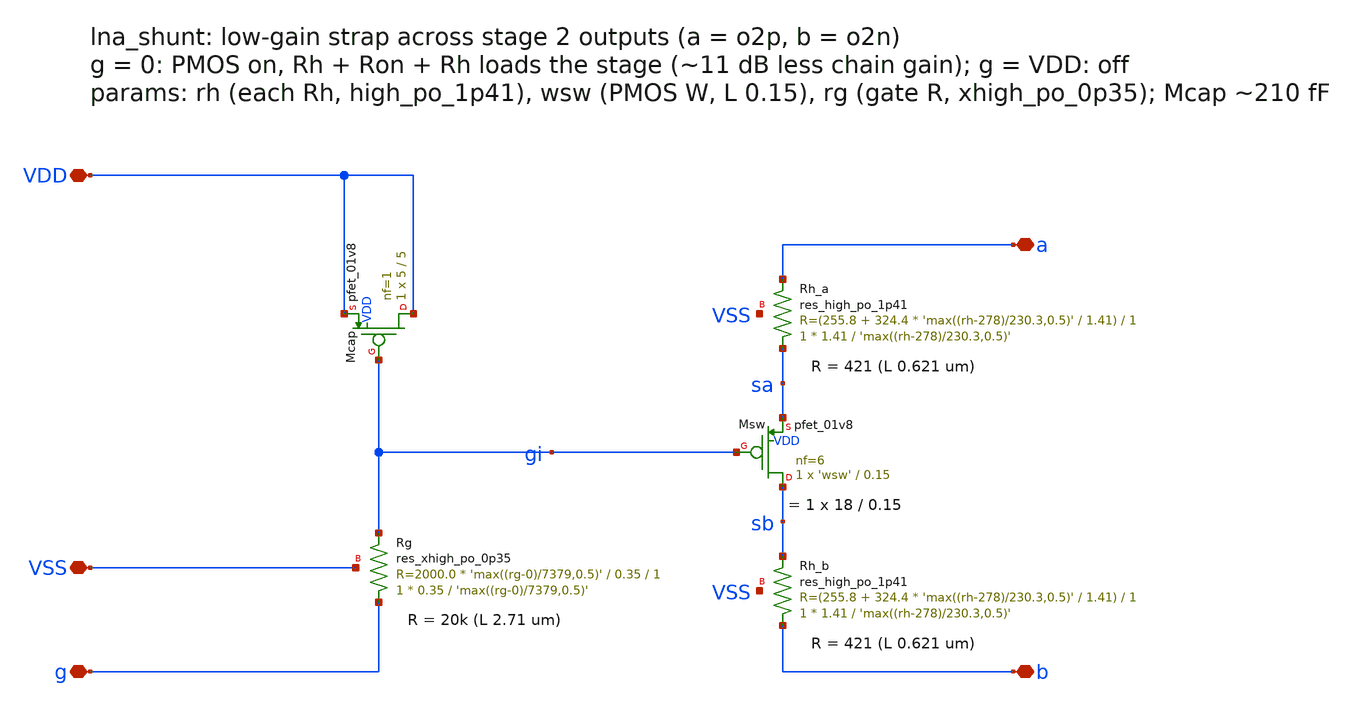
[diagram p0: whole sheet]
** sch_path: xschem/lna_shunt.sch
**.subckt lna_shunt VDD VSS a b g
*.iopin VDD
*.iopin VSS
*.iopin a
*.iopin b
*.iopin g
XRh_a sa a VSS sky130_fd_pr__res_high_po_1p41 L='max((rh-278)/230.3,0.5)' mult=1 m=1
XRh_b b sb VSS sky130_fd_pr__res_high_po_1p41 L='max((rh-278)/230.3,0.5)' mult=1 m=1
XMsw sb gi sa VDD sky130_fd_pr__pfet_01v8 L=0.15 W='wsw' nf=6 ad='int((nf+1)/2) * W/nf * 0.29' as='int((nf+2)/2) * W/nf * 0.29'
+ pd='2*int((nf+1)/2) * (W/nf + 0.29)' ps='2*int((nf+2)/2) * (W/nf + 0.29)' nrd='0.29 / W' nrs='0.29 / W'
+ sa=0 sb=0 sd=0 mult=1 m=1
XRg g gi VSS sky130_fd_pr__res_xhigh_po_0p35 L='max((rg-0)/7379,0.5)' mult=1 m=1
XMcap VDD gi VDD VDD sky130_fd_pr__pfet_01v8 L=5 W=5 nf=1 ad='int((nf+1)/2) * W/nf * 0.29' as='int((nf+2)/2) * W/nf * 0.29'
+ pd='2*int((nf+1)/2) * (W/nf + 0.29)' ps='2*int((nf+2)/2) * (W/nf + 0.29)' nrd='0.29 / W' nrs='0.29 / W'
+ sa=0 sb=0 sd=0 mult=1 m=1
**.ends
.end
